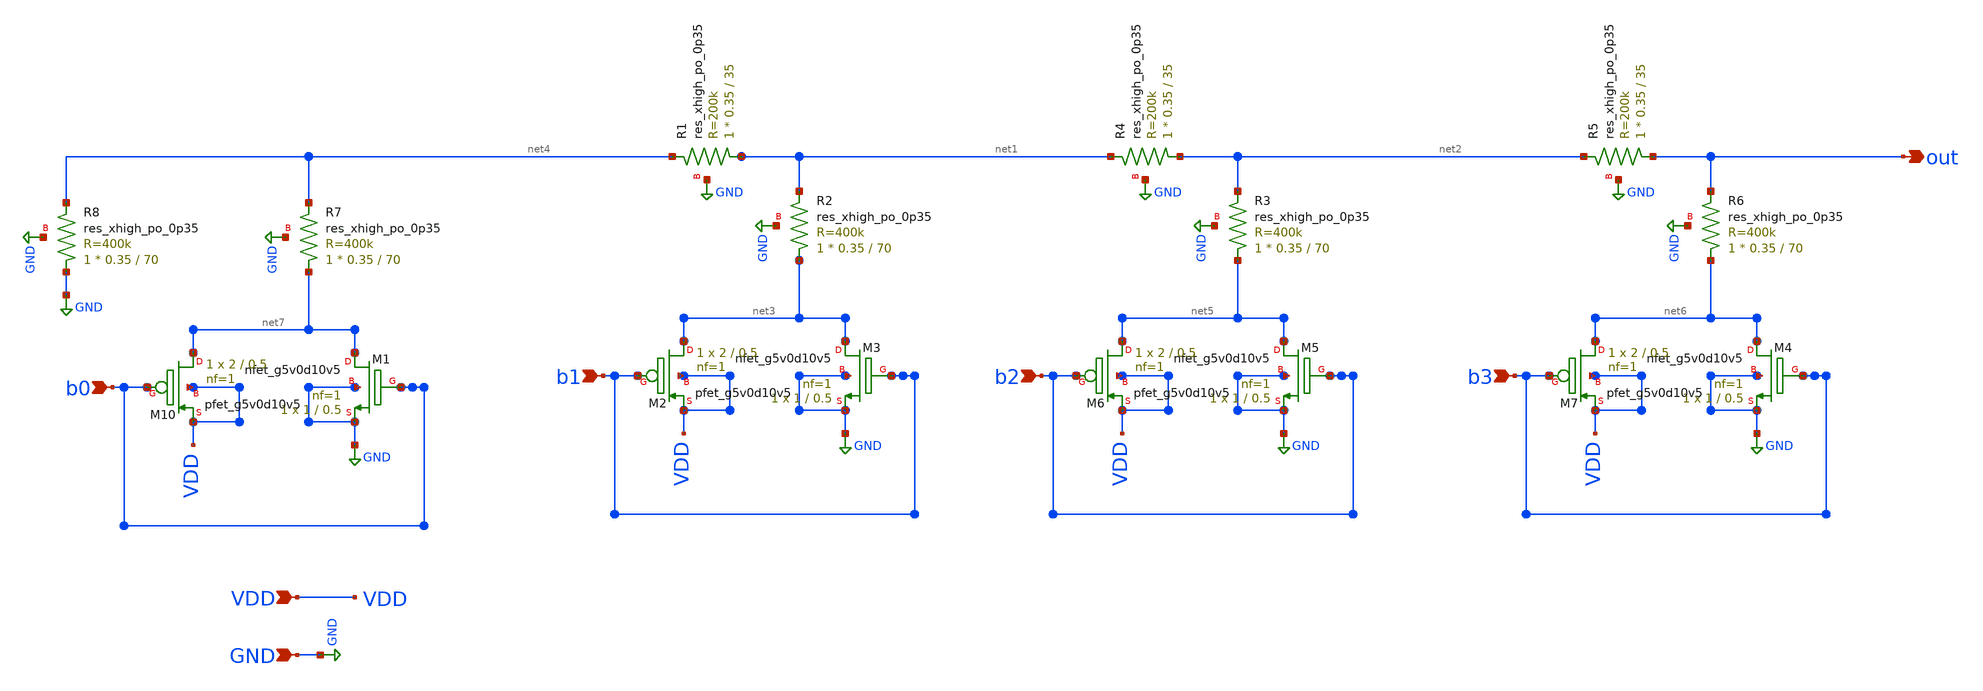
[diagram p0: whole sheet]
** sch_path: ADC/4bit_C2C/MagicAndSpice/EE431_FinalProj/R2R_20k.sch
**.subckt R2R_20k b1 b2 VDD b0 out b3 GND
*.ipin b1
*.ipin b2
*.ipin VDD
*.ipin b0
*.opin out
*.ipin b3
*.ipin GND
XR2 net3 net1 GND sky130_fd_pr__res_xhigh_po_0p35 L=70 mult=1 m=1
XR1 net1 net4 GND sky130_fd_pr__res_xhigh_po_0p35 L=35 mult=1 m=1
XR3 net5 net2 GND sky130_fd_pr__res_xhigh_po_0p35 L=70 mult=1 m=1
XR4 net2 net1 GND sky130_fd_pr__res_xhigh_po_0p35 L=35 mult=1 m=1
XR5 out net2 GND sky130_fd_pr__res_xhigh_po_0p35 L=35 mult=1 m=1
XR6 net6 out GND sky130_fd_pr__res_xhigh_po_0p35 L=70 mult=1 m=1
XR7 net7 net4 GND sky130_fd_pr__res_xhigh_po_0p35 L=70 mult=1 m=1
XR8 GND net4 GND sky130_fd_pr__res_xhigh_po_0p35 L=70 mult=1 m=1
XM1 net7 b0 GND GND sky130_fd_pr__nfet_g5v0d10v5 L=0.5 W=1 nf=1 ad='int((nf+1)/2) * W/nf * 0.29' as='int((nf+2)/2) * W/nf * 0.29'
+ pd='2*int((nf+1)/2) * (W/nf + 0.29)' ps='2*int((nf+2)/2) * (W/nf + 0.29)' nrd='0.29 / W' nrs='0.29 / W'
+ sa=0 sb=0 sd=0 mult=1 m=1
XM3 net3 b1 GND GND sky130_fd_pr__nfet_g5v0d10v5 L=0.5 W=1 nf=1 ad='int((nf+1)/2) * W/nf * 0.29' as='int((nf+2)/2) * W/nf * 0.29'
+ pd='2*int((nf+1)/2) * (W/nf + 0.29)' ps='2*int((nf+2)/2) * (W/nf + 0.29)' nrd='0.29 / W' nrs='0.29 / W'
+ sa=0 sb=0 sd=0 mult=1 m=1
XM4 net6 b3 GND GND sky130_fd_pr__nfet_g5v0d10v5 L=0.5 W=1 nf=1 ad='int((nf+1)/2) * W/nf * 0.29' as='int((nf+2)/2) * W/nf * 0.29'
+ pd='2*int((nf+1)/2) * (W/nf + 0.29)' ps='2*int((nf+2)/2) * (W/nf + 0.29)' nrd='0.29 / W' nrs='0.29 / W'
+ sa=0 sb=0 sd=0 mult=1 m=1
XM5 net5 b2 GND GND sky130_fd_pr__nfet_g5v0d10v5 L=0.5 W=1 nf=1 ad='int((nf+1)/2) * W/nf * 0.29' as='int((nf+2)/2) * W/nf * 0.29'
+ pd='2*int((nf+1)/2) * (W/nf + 0.29)' ps='2*int((nf+2)/2) * (W/nf + 0.29)' nrd='0.29 / W' nrs='0.29 / W'
+ sa=0 sb=0 sd=0 mult=1 m=1
XM10 net7 b0 VDD VDD sky130_fd_pr__pfet_g5v0d10v5 L=0.5 W=2 nf=1 ad='int((nf+1)/2) * W/nf * 0.29' as='int((nf+2)/2) * W/nf * 0.29'
+ pd='2*int((nf+1)/2) * (W/nf + 0.29)' ps='2*int((nf+2)/2) * (W/nf + 0.29)' nrd='0.29 / W' nrs='0.29 / W'
+ sa=0 sb=0 sd=0 mult=1 m=1
XM2 net3 b1 VDD VDD sky130_fd_pr__pfet_g5v0d10v5 L=0.5 W=2 nf=1 ad='int((nf+1)/2) * W/nf * 0.29' as='int((nf+2)/2) * W/nf * 0.29'
+ pd='2*int((nf+1)/2) * (W/nf + 0.29)' ps='2*int((nf+2)/2) * (W/nf + 0.29)' nrd='0.29 / W' nrs='0.29 / W'
+ sa=0 sb=0 sd=0 mult=1 m=1
XM6 net5 b2 VDD VDD sky130_fd_pr__pfet_g5v0d10v5 L=0.5 W=2 nf=1 ad='int((nf+1)/2) * W/nf * 0.29' as='int((nf+2)/2) * W/nf * 0.29'
+ pd='2*int((nf+1)/2) * (W/nf + 0.29)' ps='2*int((nf+2)/2) * (W/nf + 0.29)' nrd='0.29 / W' nrs='0.29 / W'
+ sa=0 sb=0 sd=0 mult=1 m=1
XM7 net6 b3 VDD VDD sky130_fd_pr__pfet_g5v0d10v5 L=0.5 W=2 nf=1 ad='int((nf+1)/2) * W/nf * 0.29' as='int((nf+2)/2) * W/nf * 0.29'
+ pd='2*int((nf+1)/2) * (W/nf + 0.29)' ps='2*int((nf+2)/2) * (W/nf + 0.29)' nrd='0.29 / W' nrs='0.29 / W'
+ sa=0 sb=0 sd=0 mult=1 m=1
**.ends
.GLOBAL GND
.end
